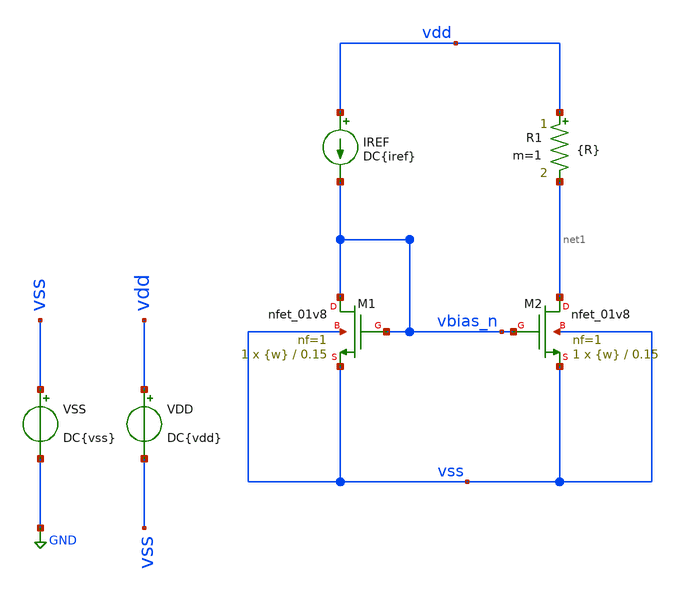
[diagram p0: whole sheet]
** sch_path: tp2/tp2_1.sch
**.subckt tp2_1
XM1 vbias_n vbias_n vss vss sky130_fd_pr__nfet_01v8 L=0.15 W={w} nf=1 ad='int((nf+1)/2) * W/nf * 0.29'
+ as='int((nf+2)/2) * W/nf * 0.29' pd='2*int((nf+1)/2) * (W/nf + 0.29)' ps='2*int((nf+2)/2) * (W/nf + 0.29)'
+ nrd='0.29 / W' nrs='0.29 / W' sa=0 sb=0 sd=0 mult=1 m=1
XM2 net1 vbias_n vss vss sky130_fd_pr__nfet_01v8 L=0.15 W={w} nf=1 ad='int((nf+1)/2) * W/nf * 0.29' as='int((nf+2)/2) * W/nf * 0.29'
+ pd='2*int((nf+1)/2) * (W/nf + 0.29)' ps='2*int((nf+2)/2) * (W/nf + 0.29)' nrd='0.29 / W' nrs='0.29 / W'
+ sa=0 sb=0 sd=0 mult=1 m=1
R1 vdd net1 {R} m=1
IREF vdd vbias_n DC{iref}
VSS vss GND DC{vss}
VDD vdd vss DC{vdd}
**** begin user architecture code



* Parameters
.param vdd = 1.8
.param vss = 0.0
.param iref = 200u
.param w = 1
.param R = 4.5k
.options TEMPS = 27.0

* Models
.lib ~/skywater/skywater-pdk/libraries/sky130_fd_pr_ngspice/latest/models/corners/sky130.lib TT

* Data to save
.save all  @M.XM1.msky130_fd_pr__nfet_01v8[id]  @M.XM1.msky130_fd_pr__nfet_01v8[gm]  @M.XM1.msky130_fd_pr__nfet_01v8[vds]  @M.XM1.msky130_fd_pr__nfet_01v8[vgs]  @M.XM1.msky130_fd_pr__nfet_01v8[w]  @M.XM2.msky130_fd_pr__nfet_01v8[id]  @M.XM2.msky130_fd_pr__nfet_01v8[gm]  @M.XM2.msky130_fd_pr__nfet_01v8[vds]  @M.XM2.msky130_fd_pr__nfet_01v8[vgs]  @M.XM2.msky130_fd_pr__nfet_01v8[w]

* Simulation
.control

  op
  save all
  unset filetype
  write tp2_1.raw

.endc

.end


**** end user architecture code
**.ends
.GLOBAL GND
.end
